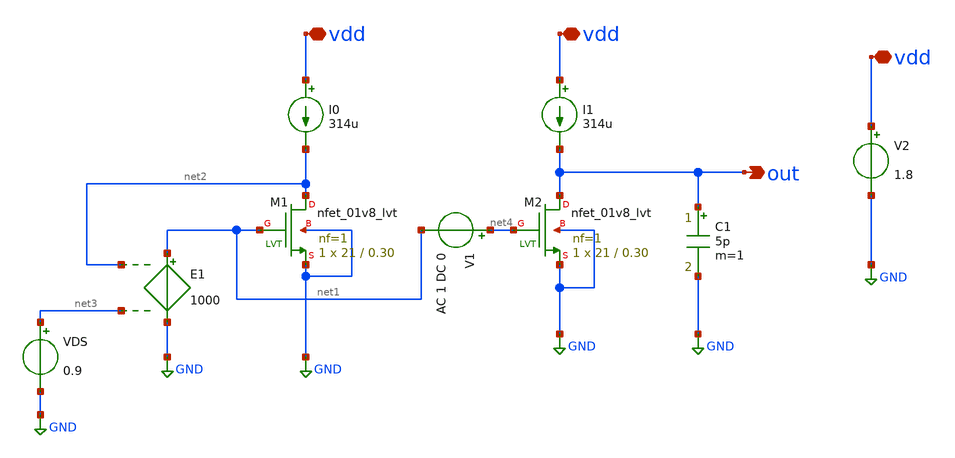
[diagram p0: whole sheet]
** sch_path: Simple-CS-Amplifier/csamp1.sch
**.subckt csamp1 vdd vdd vdd out
*.iopin vdd
*.iopin vdd
*.iopin vdd
*.opin out
XM1 net2 net1 GND GND sky130_fd_pr__nfet_01v8_lvt L=0.30 W=21 nf=1 ad='int((nf+1)/2) * W/nf * 0.29' as='int((nf+2)/2) * W/nf * 0.29'
+ pd='2*int((nf+1)/2) * (W/nf + 0.29)' ps='2*int((nf+2)/2) * (W/nf + 0.29)' nrd='0.29 / W' nrs='0.29 / W'
+ sa=0 sb=0 sd=0 mult=1 m=1
E1 net1 GND net2 net3 1000
I0 vdd net2 314u
VDS net3 GND 0.9
V2 vdd GND 1.8
XM2 out net4 GND GND sky130_fd_pr__nfet_01v8_lvt L=0.30 W=21 nf=1 ad='int((nf+1)/2) * W/nf * 0.29' as='int((nf+2)/2) * W/nf * 0.29'
+ pd='2*int((nf+1)/2) * (W/nf + 0.29)' ps='2*int((nf+2)/2) * (W/nf + 0.29)' nrd='0.29 / W' nrs='0.29 / W'
+ sa=0 sb=0 sd=0 mult=1 m=1
I1 vdd out 314u
V1 net4 net1 AC 1 DC 0
C1 out GND 5p m=1
**** begin user architecture code



.lib /usr/local/share/pdk/sky130A/libs.tech/ngspice/sky130.lib.spice tt
.option wnflag=1 scale=1e-6

.control
save all


save @m.xm2.msky130_fd_pr__nfet_01v8_lvt[vgs]
save @m.xm2.msky130_fd_pr__nfet_01v8_lvt[vds]
save @m.xm2.msky130_fd_pr__nfet_01v8_lvt[gm]
save @m.xm2.msky130_fd_pr__nfet_01v8_lvt[ro]


dc V1 0 1.8 1m


let vgs = @m.xm2.msky130_fd_pr__nfet_01v8_lvt[vgs]
let vds = @m.xm2.msky130_fd_pr__nfet_01v8_lvt[vds]
let gm = @m.xm2.msky130_fd_pr__nfet_01v8_lvt[gm]
let ro = @m.xm2.msky130_fd_pr__nfet_01v8_lvt[ro]

*let a = deriv(vgs)
*let ao = -1/a

plot gm*ro

*tran 10u 10m

plot v(out)


*wrdata ao-L=0.40.txt ao
.endc


**** end user architecture code
**.ends
.GLOBAL GND
.end
